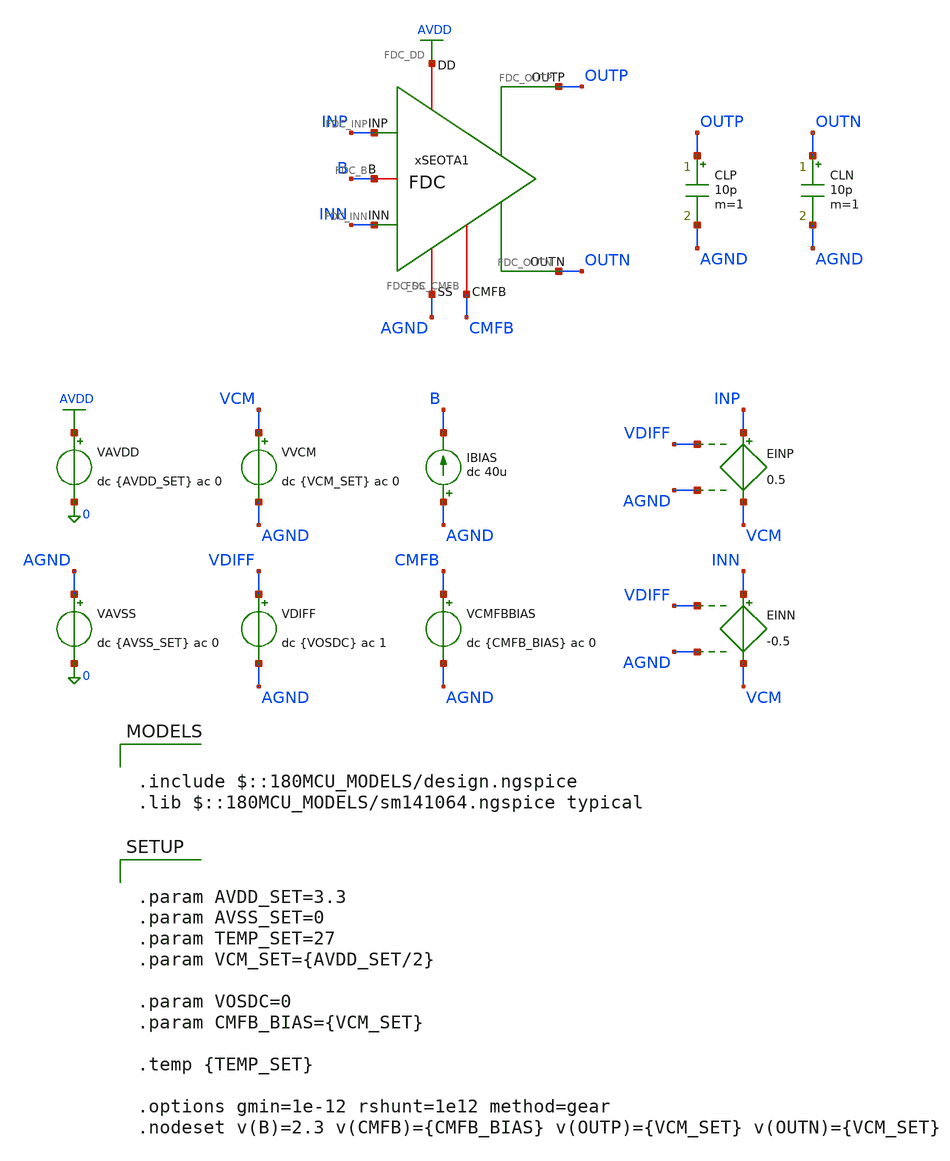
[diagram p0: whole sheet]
** sch_path: Design_Files/IC Design/Testbench/FD_OTA/FDC/Open_Loop/FDC_TB_VCMFB_NOM.sch
**.subckt FDC_TB_VCMFB_NOM
IBIAS AGND B dc 40u
VAVDD AVDD 0 dc {AVDD_SET} ac 0
.save i(vavdd)
CLP OUTP AGND 10p m=1
VVCM VCM AGND dc {VCM_SET} ac 0
VDIFF VDIFF AGND dc {VOSDC} ac 1
VAVSS AGND 0 dc {AVSS_SET} ac 0
.save i(vavss)
EINN INN VCM VDIFF AGND -0.5
EINP INP VCM VDIFF AGND 0.5
xSEOTA1 AVDD AGND INP INN OUTN B OUTP CMFB FDC
CLN OUTN AGND 10p m=1
VCMFBBIAS CMFB AGND dc {CMFB_BIAS} ac 0
**** begin user architecture code

.include $::180MCU_MODELS/design.ngspice
.lib $::180MCU_MODELS/sm141064.ngspice typical



.control
destroy all
save all
set wr_vecnames
set wr_singlescale
option numdgt=15

shell mkdir -p
+ /foss/designs/ECG_Acquisition_IC/Measurement_Results/IC_Simulation/FD_OTA/FDC/NOM.Result_txt

shell rm -f
+ /foss/designs/ECG_Acquisition_IC/Measurement_Results/IC_Simulation/FD_OTA/FDC/NOM.Result_txt/NOM.vcmfb_sweep.txt

let avdd_run = 3.3
let vcm_run  = avdd_run/2
let vos_run  = 0

alter @VAVDD[DC] = $&avdd_run
alter @VVCM[DC]  = $&vcm_run
alter @VDIFF[DC] = $&vos_run

alter @VVCM[ACMAG]  = 0
alter @VDIFF[ACMAG] = 0
alter @VAVDD[ACMAG] = 0
alter @VAVSS[ACMAG] = 0

* VCMFB sweep
dc VCMFBBIAS 0 $&avdd_run 1e-4

let sweep_vcmfb  = v(cmfb)-v(agnd)
let sweep_voutp  = v(outp)-v(agnd)
let sweep_voutn  = v(outn)-v(agnd)
let sweep_voutcm = (sweep_voutp+sweep_voutn)/2
let sweep_vod    = sweep_voutp-sweep_voutn

setscale sweep_vcmfb

wrdata
+ /foss/designs/ECG_Acquisition_IC/Measurement_Results/IC_Simulation/FD_OTA/FDC/NOM.Result_txt/NOM.vcmfb_sweep.txt sweep_voutp sweep_voutn sweep_voutcm sweep_vod

.endc




.param AVDD_SET=3.3
.param AVSS_SET=0
.param TEMP_SET=27
.param VCM_SET={AVDD_SET/2}

.param VOSDC=0
.param CMFB_BIAS={VCM_SET}

.temp {TEMP_SET}

.options gmin=1e-12 rshunt=1e12 method=gear
.nodeset v(B)=2.3 v(CMFB)={CMFB_BIAS} v(OUTP)={VCM_SET} v(OUTN)={VCM_SET}


**** end user architecture code
**.ends

* expanding   symbol:  ECG_Acquisition_IC/Design_Files/IC Design/Schematic/FD_OTA/FDC/FDC.sym # of
*+ pins=8
** sym_path: Design_Files/IC Design/Schematic/FD_OTA/FDC/FDC.sym
** sch_path: Design_Files/IC Design/Schematic/FD_OTA/FDC/FDC.sch
.subckt FDC FDC_DD FDC_SS FDC_INP FDC_INN FDC_OUTN FDC_B FDC_OUTP FDC_CMFB
*.iopin FDC_DD
*.iopin FDC_SS
*.ipin FDC_INP
*.ipin FDC_INN
*.opin FDC_OUTP
*.iopin FDC_B
*.opin FDC_OUTN
*.iopin FDC_CMFB
XM3 net4 FDC_CMFB FDC_DD FDC_DD pfet_03v3 L=2u W=1u nf=1 ad='int((nf+1)/2) * W/nf * 0.18u' as='int((nf+2)/2) * W/nf * 0.18u'
+ pd='2*int((nf+1)/2) * (W/nf + 0.18u)' ps='2*int((nf+2)/2) * (W/nf + 0.18u)' nrd='0.18u / W' nrs='0.18u / W'
+ sa=0 sb=0 sd=0 m=200
XM8 FDC_OUTP FDC_B FDC_SS FDC_SS nfet_03v3 L=0.5u W=1u nf=1 ad='int((nf+1)/2) * W/nf * 0.18u' as='int((nf+2)/2) * W/nf * 0.18u'
+ pd='2*int((nf+1)/2) * (W/nf + 0.18u)' ps='2*int((nf+2)/2) * (W/nf + 0.18u)' nrd='0.18u / W' nrs='0.18u / W'
+ sa=0 sb=0 sd=0 m=120
Rz net1 net2 2k m=1
XM5 net3 FDC_B FDC_SS FDC_SS nfet_03v3 L=2u W=1u nf=1 ad='int((nf+1)/2) * W/nf * 0.18u' as='int((nf+2)/2) * W/nf * 0.18u'
+ pd='2*int((nf+1)/2) * (W/nf + 0.18u)' ps='2*int((nf+2)/2) * (W/nf + 0.18u)' nrd='0.18u / W' nrs='0.18u / W'
+ sa=0 sb=0 sd=0 m=20
XM6 FDC_OUTP net1 FDC_DD FDC_DD pfet_03v3 L=0.5u W=1u nf=1 ad='int((nf+1)/2) * W/nf * 0.18u' as='int((nf+2)/2) * W/nf * 0.18u'
+ pd='2*int((nf+1)/2) * (W/nf + 0.18u)' ps='2*int((nf+2)/2) * (W/nf + 0.18u)' nrd='0.18u / W' nrs='0.18u / W'
+ sa=0 sb=0 sd=0 m=400
XM10 FDC_B FDC_B FDC_SS FDC_SS nfet_03v3 L=2u W=1u nf=1 ad='int((nf+1)/2) * W/nf * 0.18u' as='int((nf+2)/2) * W/nf * 0.18u'
+ pd='2*int((nf+1)/2) * (W/nf + 0.18u)' ps='2*int((nf+2)/2) * (W/nf + 0.18u)' nrd='0.18u / W' nrs='0.18u / W'
+ sa=0 sb=0 sd=0 m=50
Cc net2 FDC_OUTP 2p m=1
XM9 FDC_OUTN FDC_B FDC_SS FDC_SS nfet_03v3 L=0.5u W=1u nf=1 ad='int((nf+1)/2) * W/nf * 0.18u' as='int((nf+2)/2) * W/nf * 0.18u'
+ pd='2*int((nf+1)/2) * (W/nf + 0.18u)' ps='2*int((nf+2)/2) * (W/nf + 0.18u)' nrd='0.18u / W' nrs='0.18u / W'
+ sa=0 sb=0 sd=0 m=120
Rz1 net4 net5 2k m=1
XM7 FDC_OUTN net4 FDC_DD FDC_DD pfet_03v3 L=0.5u W=1u nf=1 ad='int((nf+1)/2) * W/nf * 0.18u' as='int((nf+2)/2) * W/nf * 0.18u'
+ pd='2*int((nf+1)/2) * (W/nf + 0.18u)' ps='2*int((nf+2)/2) * (W/nf + 0.18u)' nrd='0.18u / W' nrs='0.18u / W'
+ sa=0 sb=0 sd=0 m=400
Cc1 net5 FDC_OUTN 2p m=1
XM4 net1 FDC_CMFB FDC_DD FDC_DD pfet_03v3 L=2u W=1u nf=1 ad='int((nf+1)/2) * W/nf * 0.18u' as='int((nf+2)/2) * W/nf * 0.18u'
+ pd='2*int((nf+1)/2) * (W/nf + 0.18u)' ps='2*int((nf+2)/2) * (W/nf + 0.18u)' nrd='0.18u / W' nrs='0.18u / W'
+ sa=0 sb=0 sd=0 m=200
XM1 net4 FDC_INN net3 FDC_SS nfet_03v3 L=2u W=1u nf=1 ad='int((nf+1)/2) * W/nf * 0.18u' as='int((nf+2)/2) * W/nf * 0.18u'
+ pd='2*int((nf+1)/2) * (W/nf + 0.18u)' ps='2*int((nf+2)/2) * (W/nf + 0.18u)' nrd='0.18u / W' nrs='0.18u / W'
+ sa=0 sb=0 sd=0 m=400
XM2 net1 FDC_INP net3 FDC_SS nfet_03v3 L=2u W=1u nf=1 ad='int((nf+1)/2) * W/nf * 0.18u' as='int((nf+2)/2) * W/nf * 0.18u'
+ pd='2*int((nf+1)/2) * (W/nf + 0.18u)' ps='2*int((nf+2)/2) * (W/nf + 0.18u)' nrd='0.18u / W' nrs='0.18u / W'
+ sa=0 sb=0 sd=0 m=400
.ends

.GLOBAL AVDD
.end
